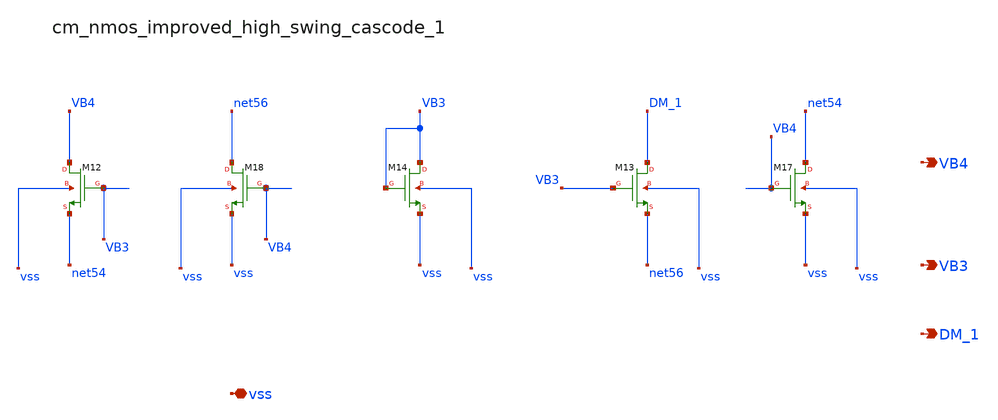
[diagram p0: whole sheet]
** sch_path: analog-db/raw/amp_008_leung_nmcf/hier/blocks/cm_nmos_improved_high_swing_cascode_1.sch
**.subckt cm_nmos_improved_high_swing_cascode_1 vss VB4 VB3 DM_1
*.iopin vss
*.opin VB4
*.opin VB3
*.opin DM_1
XM12 VB4 VB3 net54 vss sg13_lv_nmos w=x_dut_xm12_w l=x_dut_xm12_l ng=1 m=x_dut_xm12_m
XM13 DM_1 VB3 net56 vss sg13_lv_nmos w=x_dut_xm13_w l=x_dut_xm13_l ng=1 m=x_dut_xm13_m
XM14 VB3 VB3 vss vss sg13_lv_nmos w=x_dut_xm14_w l=x_dut_xm14_l ng=1 m=x_dut_xm14_m
XM17 net54 VB4 vss vss sg13_lv_nmos w=x_dut_xm17_w l=x_dut_xm17_l ng=1 m=x_dut_xm17_m
XM18 net56 VB4 vss vss sg13_lv_nmos w=x_dut_xm18_w l=x_dut_xm18_l ng=1 m=x_dut_xm18_m
**.ends
.end
